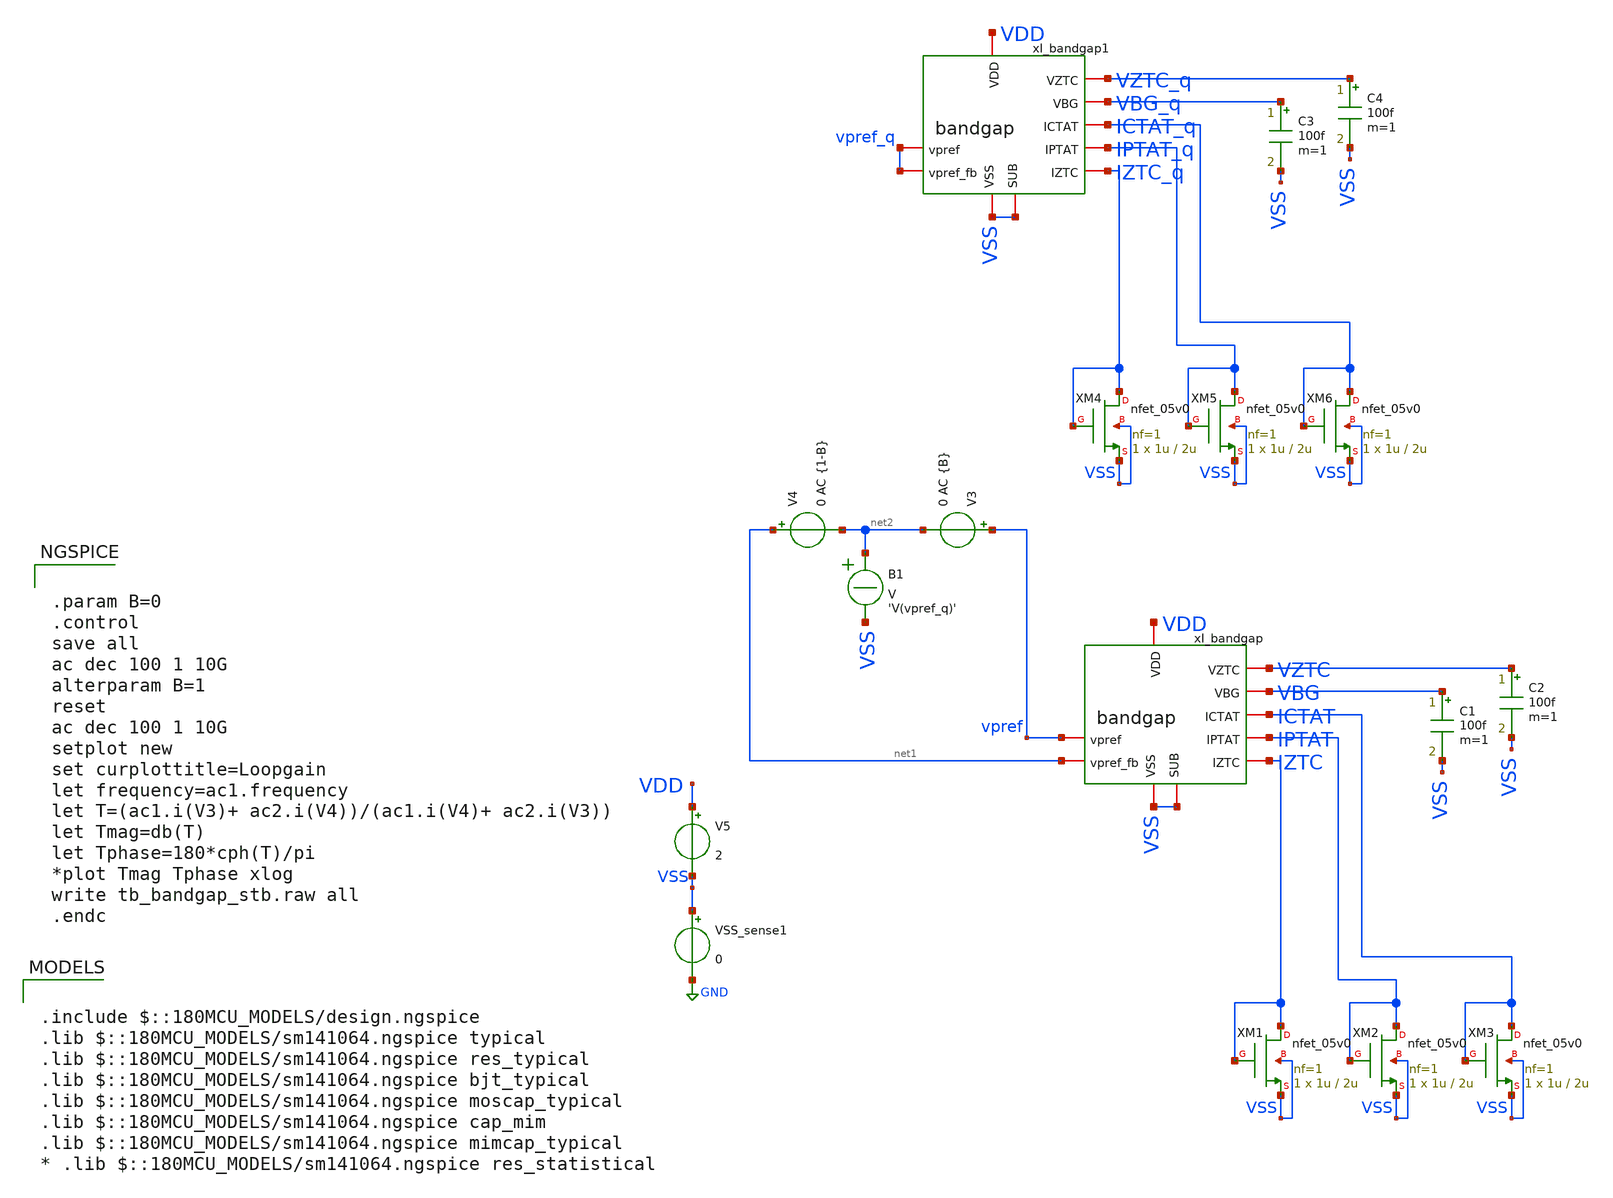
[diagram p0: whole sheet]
** sch_path: designs/libs/tb_bandgap/tb_bandgap_stb/tb_bandgap_stb.sch
**.subckt tb_bandgap_stb
V4 net1 net2 0 AC {1-B}
B1 net2 VSS V = 'V(vpref_q)'
V3 vpref net2 0 AC {B}
V5 VDD VSS 2
VSS_sense1 VSS GND 0
C1 VBG VSS 100f m=1
xI_bandgap VDD VBG IPTAT IZTC VSS VSS vpref net1 ICTAT VZTC bandgap
C2 VZTC VSS 100f m=1
XM1 IZTC IZTC VSS VSS nfet_05v0 L=2u W=1u nf=1 ad='int((nf+1)/2) * W/nf * 0.18u' as='int((nf+2)/2) * W/nf * 0.18u'
+ pd='2*int((nf+1)/2) * (W/nf + 0.18u)' ps='2*int((nf+2)/2) * (W/nf + 0.18u)' nrd='0.18u / W' nrs='0.18u / W'
+ sa=0 sb=0 sd=0 m=1
XM2 IPTAT IPTAT VSS VSS nfet_05v0 L=2u W=1u nf=1 ad='int((nf+1)/2) * W/nf * 0.18u' as='int((nf+2)/2) * W/nf * 0.18u'
+ pd='2*int((nf+1)/2) * (W/nf + 0.18u)' ps='2*int((nf+2)/2) * (W/nf + 0.18u)' nrd='0.18u / W' nrs='0.18u / W'
+ sa=0 sb=0 sd=0 m=1
XM3 ICTAT ICTAT VSS VSS nfet_05v0 L=2u W=1u nf=1 ad='int((nf+1)/2) * W/nf * 0.18u' as='int((nf+2)/2) * W/nf * 0.18u'
+ pd='2*int((nf+1)/2) * (W/nf + 0.18u)' ps='2*int((nf+2)/2) * (W/nf + 0.18u)' nrd='0.18u / W' nrs='0.18u / W'
+ sa=0 sb=0 sd=0 m=1
C3 VBG_q VSS 100f m=1
xI_bandgap1 VDD VBG_q IPTAT_q IZTC_q VSS VSS vpref_q vpref_q ICTAT_q VZTC_q bandgap
C4 VZTC_q VSS 100f m=1
XM4 IZTC_q IZTC_q VSS VSS nfet_05v0 L=2u W=1u nf=1 ad='int((nf+1)/2) * W/nf * 0.18u' as='int((nf+2)/2) * W/nf * 0.18u'
+ pd='2*int((nf+1)/2) * (W/nf + 0.18u)' ps='2*int((nf+2)/2) * (W/nf + 0.18u)' nrd='0.18u / W' nrs='0.18u / W'
+ sa=0 sb=0 sd=0 m=1
XM5 IPTAT_q IPTAT_q VSS VSS nfet_05v0 L=2u W=1u nf=1 ad='int((nf+1)/2) * W/nf * 0.18u' as='int((nf+2)/2) * W/nf * 0.18u'
+ pd='2*int((nf+1)/2) * (W/nf + 0.18u)' ps='2*int((nf+2)/2) * (W/nf + 0.18u)' nrd='0.18u / W' nrs='0.18u / W'
+ sa=0 sb=0 sd=0 m=1
XM6 ICTAT_q ICTAT_q VSS VSS nfet_05v0 L=2u W=1u nf=1 ad='int((nf+1)/2) * W/nf * 0.18u' as='int((nf+2)/2) * W/nf * 0.18u'
+ pd='2*int((nf+1)/2) * (W/nf + 0.18u)' ps='2*int((nf+2)/2) * (W/nf + 0.18u)' nrd='0.18u / W' nrs='0.18u / W'
+ sa=0 sb=0 sd=0 m=1
**** begin user architecture code

.include $::180MCU_MODELS/design.ngspice
.lib $::180MCU_MODELS/sm141064.ngspice typical
.lib $::180MCU_MODELS/sm141064.ngspice res_typical
.lib $::180MCU_MODELS/sm141064.ngspice bjt_typical
.lib $::180MCU_MODELS/sm141064.ngspice moscap_typical
.lib $::180MCU_MODELS/sm141064.ngspice cap_mim
.lib $::180MCU_MODELS/sm141064.ngspice mimcap_typical
* .lib $::180MCU_MODELS/sm141064.ngspice res_statistical



.param B=0
.control
save all
ac dec 100 1 10G
alterparam B=1
reset
ac dec 100 1 10G
setplot new
set curplottitle=Loopgain
let frequency=ac1.frequency
let T=(ac1.i(V3)+ ac2.i(V4))/(ac1.i(V4)+ ac2.i(V3))
let Tmag=db(T)
let Tphase=180*cph(T)/pi
*plot Tmag Tphase xlog
write tb_bandgap_stb.raw all
.endc


**** end user architecture code
**.ends
.GLOBAL GND
.end
